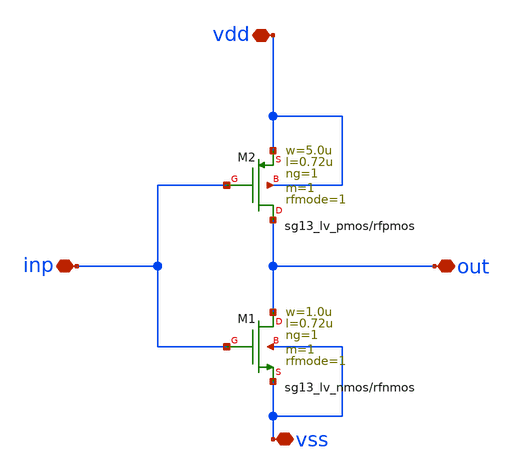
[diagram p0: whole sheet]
** sch_path: xschem/inv.sch
**.subckt inv vss out inp vdd
*.iopin vss
*.iopin out
*.iopin inp
*.iopin vdd
XM1 out inp vss vss sg13_lv_nmos w=1.0u l=0.72u ng=1 m=1 rfmode=1 mm_ok=1
XM2 out inp vdd vdd sg13_lv_pmos w=5.0u l=0.72u ng=1 m=1 rfmode=1 mm_ok=1
**.ends
.end
